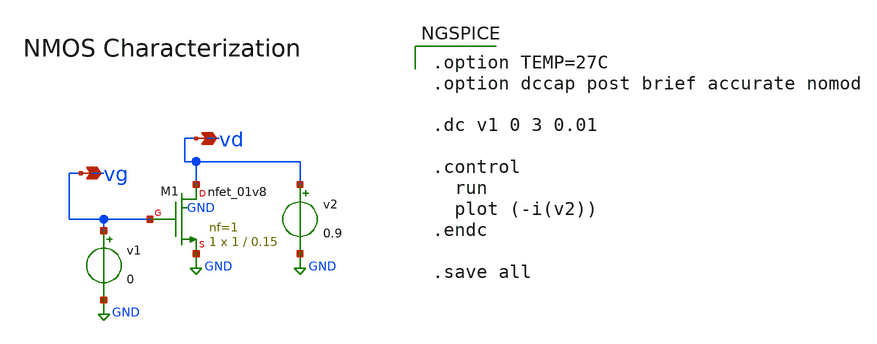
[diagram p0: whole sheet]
** sch_path: xschem/untitled.sch
**.subckt untitled vg vd
*.opin vg
*.opin vd
XM1 vd vg GND GND sky130_fd_pr__nfet_01v8 L=0.15 W=1 nf=1 ad='int((nf+1)/2) * W/nf * 0.29' as='int((nf+2)/2) * W/nf * 0.29'
+ pd='2*int((nf+1)/2) * (W/nf + 0.29)' ps='2*int((nf+2)/2) * (W/nf + 0.29)' nrd='0.29 / W' nrs='0.29 / W'
+ sa=0 sb=0 sd=0 mult=1 m=1
v1 vg GND 0
v2 vd GND 0.9
**** begin user architecture code

.option TEMP=27C
.option dccap post brief accurate nomod

.dc v1 0 3 0.01

.control
  run
  plot (-i(v2))
.endc

.save all


 ** manual skywater pdks install (with patches applied)
* .lib $::SKYWATER_MODELS/models/sky130.lib.spice tt

** opencircuitdesign pdks install
.lib $::SKYWATER_MODELS/sky130.lib.spice tt

.param mc_mm_switch=0
.param mc_pr_switch=0

**** end user architecture code
**.ends
.GLOBAL GND
.end
